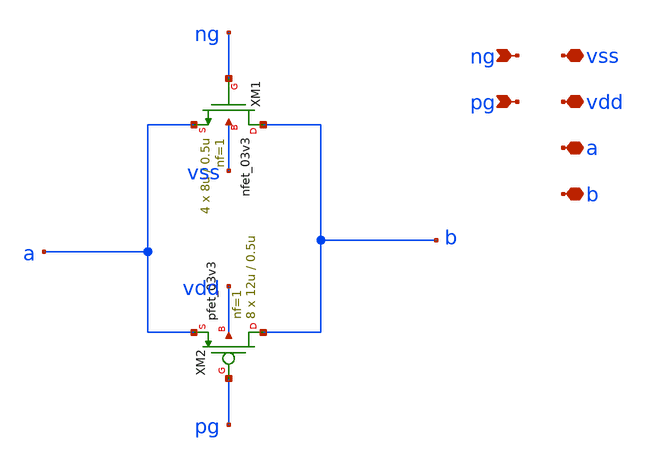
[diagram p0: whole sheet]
** sch_path: xschem/SAR_ADC/xschem/tg.sch
**.subckt tg ng vdd pg a b vss
*.ipin ng
*.iopin vdd
*.ipin pg
*.iopin a
*.iopin b
*.iopin vss
XM2 b pg a vdd pfet_03v3 L=0.5u W=12u nf=1 ad='int((nf+1)/2) * W/nf * 0.18u' as='int((nf+2)/2) * W/nf * 0.18u'
+ pd='2*int((nf+1)/2) * (W/nf + 0.18u)' ps='2*int((nf+2)/2) * (W/nf + 0.18u)' nrd='0.18u / W' nrs='0.18u / W'
+ sa=0 sb=0 sd=0 m=8
XM1 b ng a vss nfet_03v3 L=0.5u W=8u nf=1 ad='int((nf+1)/2) * W/nf * 0.18u' as='int((nf+2)/2) * W/nf * 0.18u'
+ pd='2*int((nf+1)/2) * (W/nf + 0.18u)' ps='2*int((nf+2)/2) * (W/nf + 0.18u)' nrd='0.18u / W' nrs='0.18u / W'
+ sa=0 sb=0 sd=0 m=4
**.ends
.end
